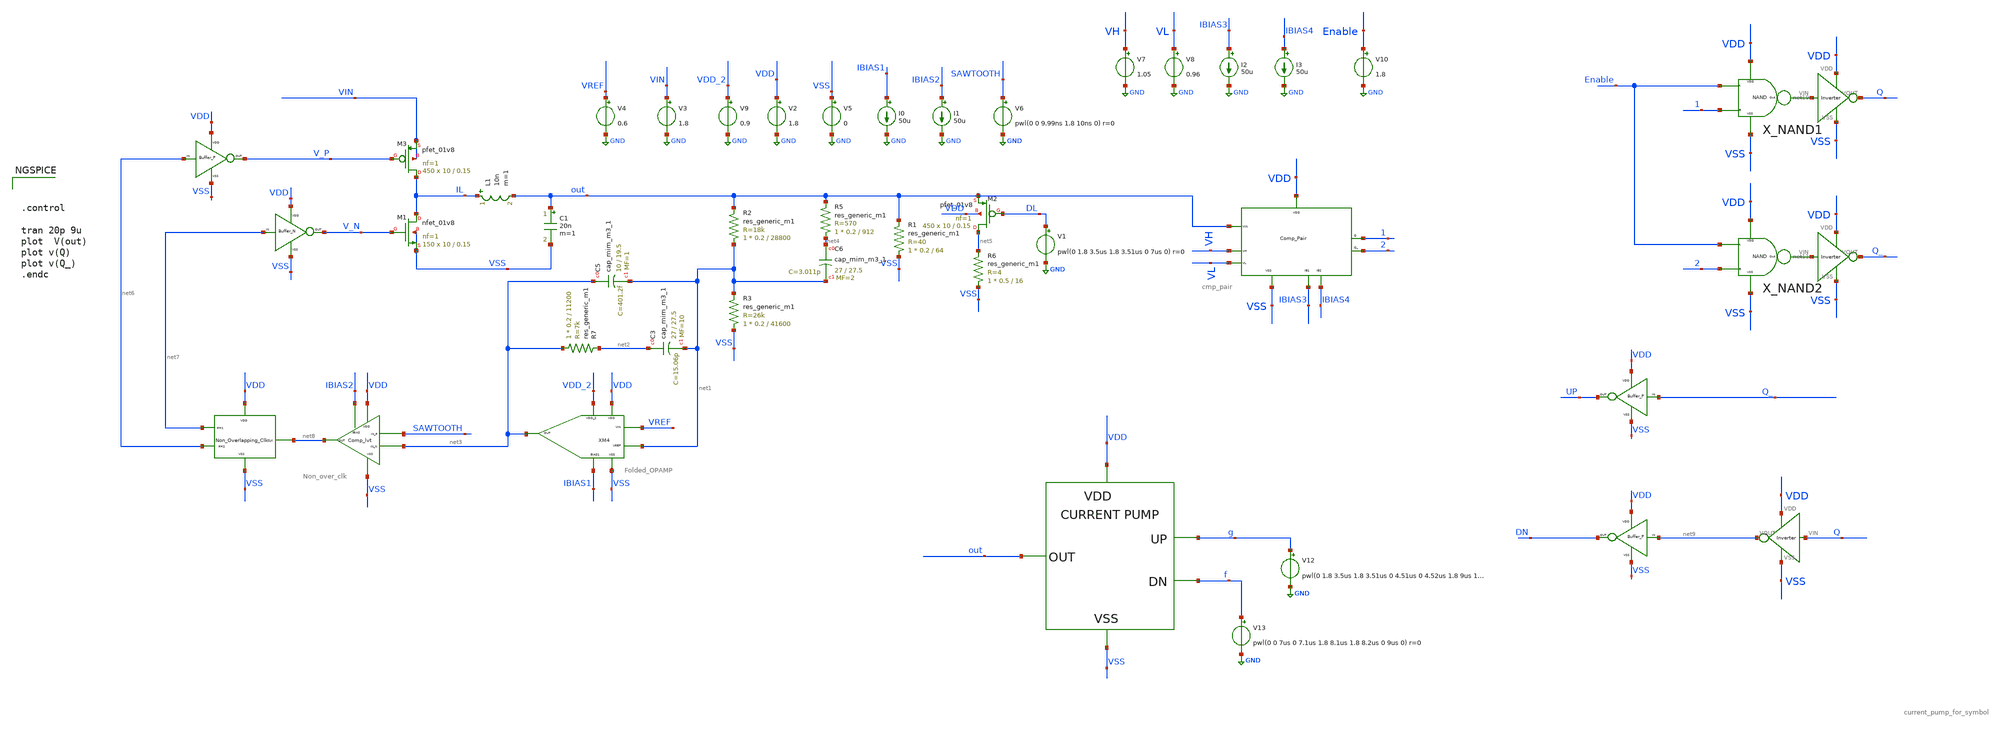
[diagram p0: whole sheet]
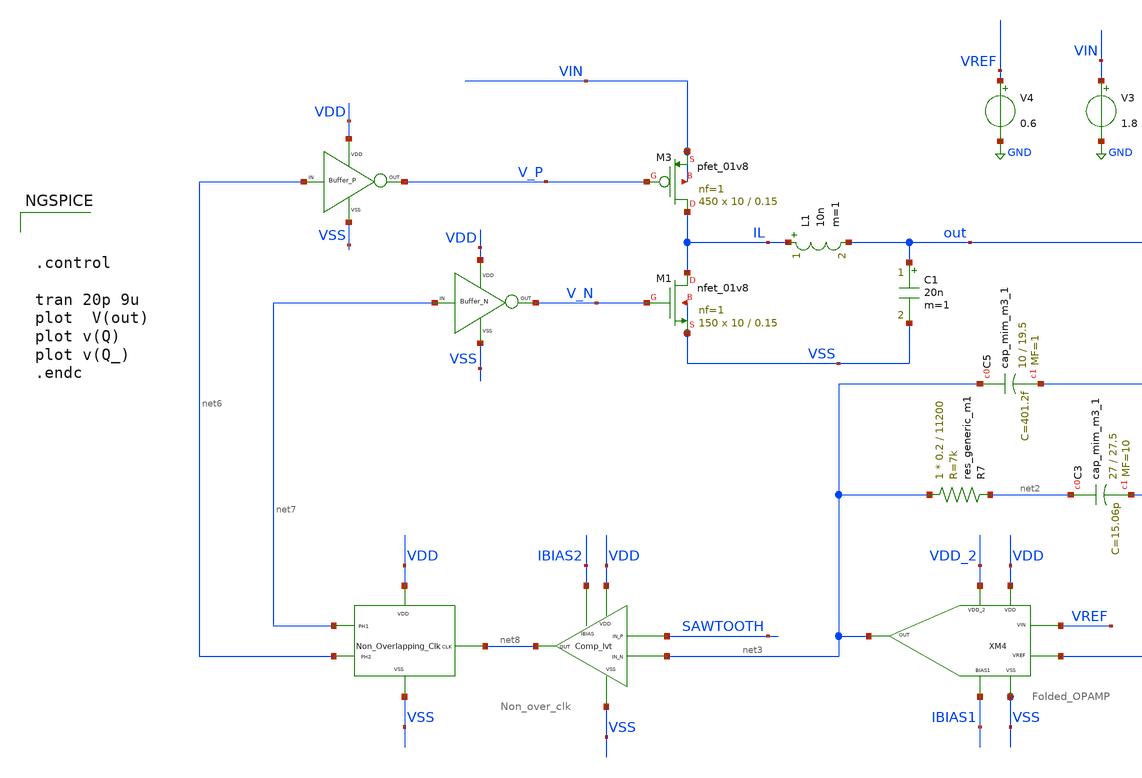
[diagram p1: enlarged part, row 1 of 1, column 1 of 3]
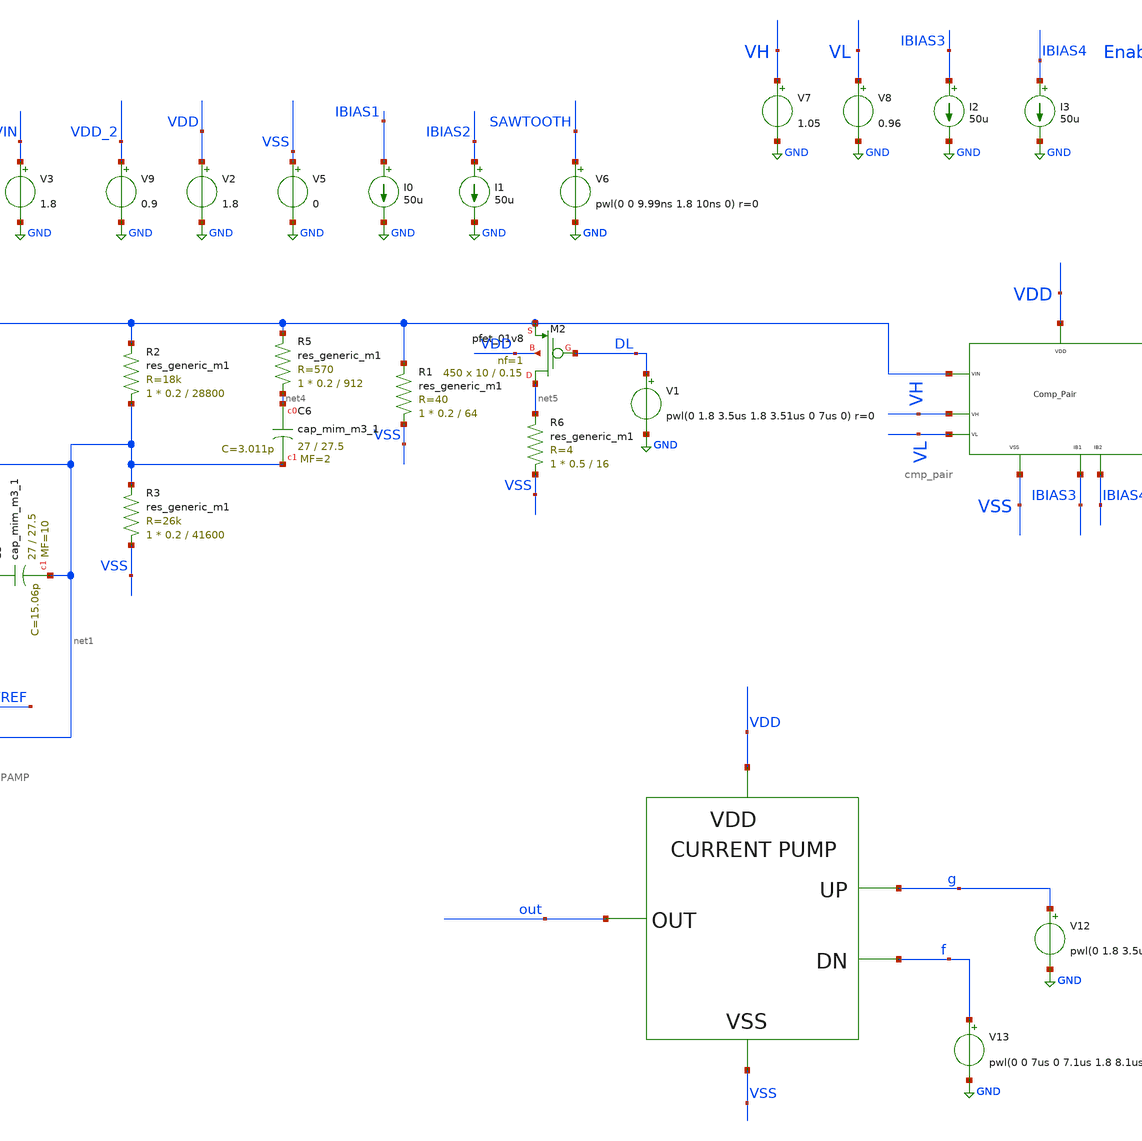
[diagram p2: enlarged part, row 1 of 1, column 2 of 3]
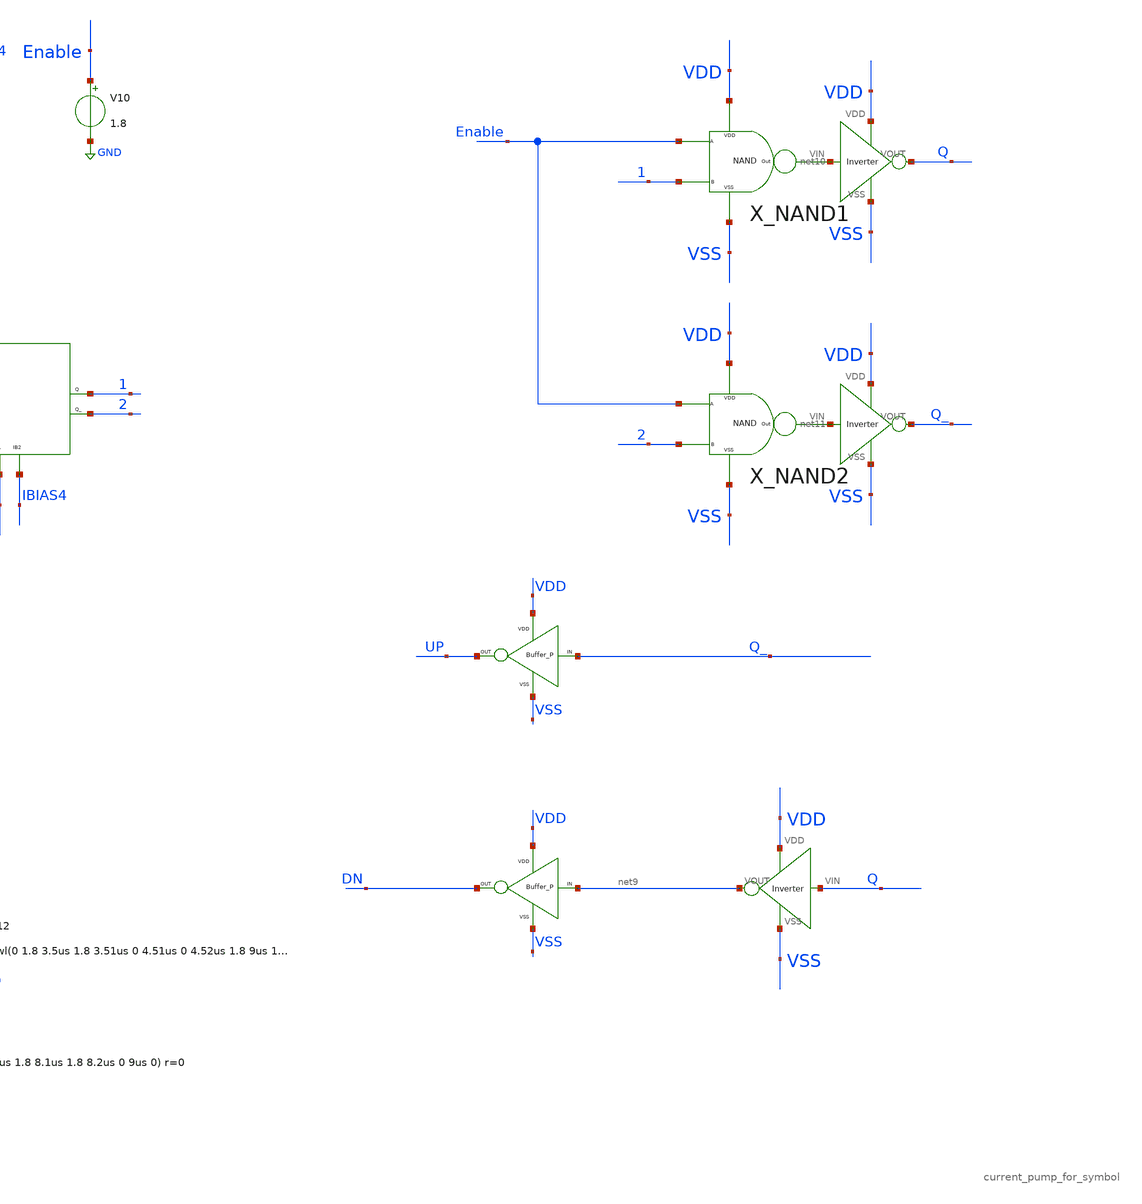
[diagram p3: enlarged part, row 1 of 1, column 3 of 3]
** sch_path: xschem/DC_DC_Converter_xschem/OTHERS/DC_DC_Converter_JV8/TOP_LEVEL/closed_loop_v8.sch
**.subckt closed_loop_v8
XM3 IL V_P VIN VIN sky130_fd_pr__pfet_01v8 L=0.15 W=10 nf=1 ad='int((nf+1)/2) * W/nf * 0.29' as='int((nf+2)/2) * W/nf * 0.29'
+ pd='2*int((nf+1)/2) * (W/nf + 0.29)' ps='2*int((nf+2)/2) * (W/nf + 0.29)' nrd='0.29 / W' nrs='0.29 / W'
+ sa=0 sb=0 sd=0 mult=450 m=450
L1 IL out 10n m=1
C1 out VSS 20n m=1
V3 VIN GND 1.8
I0 IBIAS1 GND 50u
V9 VDD_2 GND 0.9
V2 VDD GND 1.8
V5 VSS GND 0
V4 VREF GND 0.6
I1 IBIAS2 GND 50u
V6 SAWTOOTH GND pwl(0 0 9.99ns 1.8 10ns 0) r=0
XM1 IL V_N VSS VSS sky130_fd_pr__nfet_01v8 L=0.15 W=10 nf=1 ad='int((nf+1)/2) * W/nf * 0.29' as='int((nf+2)/2) * W/nf * 0.29'
+ pd='2*int((nf+1)/2) * (W/nf + 0.29)' ps='2*int((nf+2)/2) * (W/nf + 0.29)' nrd='0.29 / W' nrs='0.29 / W'
+ sa=0 sb=0 sd=0 mult=150 m=150
XM2 net5 DL out VDD sky130_fd_pr__pfet_01v8 L=0.15 W=10 nf=1 ad='int((nf+1)/2) * W/nf * 0.29' as='int((nf+2)/2) * W/nf * 0.29'
+ pd='2*int((nf+1)/2) * (W/nf + 0.29)' ps='2*int((nf+2)/2) * (W/nf + 0.29)' nrd='0.29 / W' nrs='0.29 / W'
+ sa=0 sb=0 sd=0 mult=450 m=450
V1 DL GND pwl(0 1.8 3.5us 1.8 3.51us 0 7us 0) r=0
X1 net6 V_P VDD VSS BUFFER_P
X2 net7 V_N VDD VSS BUFFER_N
XM3 net8 VDD VSS net7 net6 Non_over_clk
XM4 VDD VSS VDD_2 IBIAS1 net3 VREF net1 Folded_OPAMP
XM2 IBIAS2 VDD SAWTOOTH net3 VSS net8 Comp_lvt
V7 VH GND 1.05
V8 VL GND 0.96
I2 IBIAS3 GND 50u
I3 IBIAS4 GND 50u
XM1 VDD VSS out VH VL IBIAS3 IBIAS4 1 2 cmp_pair
X5 net9 DN VDD VSS BUFFER_P
X6 Q_ UP VDD VSS BUFFER_P
X7 g out VDD VSS f current_pump_for_symbol
X_NAND1 VDD VSS Enable 1 net10 NAND
X_NAND2 VDD VSS Enable 2 net11 NAND
X9 VSS VDD net10 Q Inverter
X10 VSS VDD net11 Q_ Inverter
XC5 net3 net1 sky130_fd_pr__cap_mim_m3_1 W=10 L=19.5 MF=1 m=1
XC3 net2 net1 sky130_fd_pr__cap_mim_m3_1 W=27 L=27.5 MF=10 m=10
R7 net3 net2 sky130_fd_pr__res_generic_m1 W=0.2 L=11200 m=1
R6 VSS net5 sky130_fd_pr__res_generic_m1 W=0.5 L=16 m=1
R1 VSS out sky130_fd_pr__res_generic_m1 W=0.2 L=64 m=1
R5 net4 out sky130_fd_pr__res_generic_m1 W=0.2 L=912 m=1
R2 net1 out sky130_fd_pr__res_generic_m1 W=0.2 L=28800 m=1
R3 VSS net1 sky130_fd_pr__res_generic_m1 W=0.2 L=41600 m=1
V10 Enable GND 1.8
XC6 net4 net1 sky130_fd_pr__cap_mim_m3_1 W=27 L=27.5 MF=2 m=2
X3 VSS VDD Q net9 Inverter
V12 g GND pwl(0 1.8 3.5us 1.8 3.51us 0 4.51us 0 4.52us 1.8 9us 1.8) r=0
V13 f GND pwl(0 0 7us 0 7.1us 1.8 8.1us 1.8 8.2us 0 9us 0) r=0
**** begin user architecture code

** opencircuitdesign pdks install
.lib $::SKYWATER_MODELS/sky130.lib.spice tt





.control

tran 20p 9u
plot  V(out)
plot v(Q)
plot v(Q_)
.endc


**** end user architecture code
**.ends
.GLOBAL GND
.end
